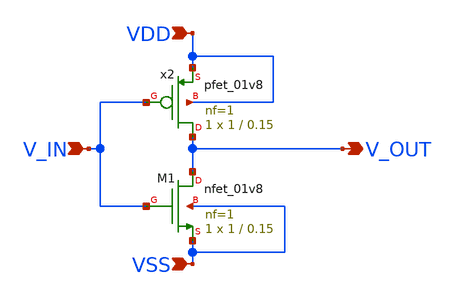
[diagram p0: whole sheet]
** sch_path: schematics_xschem/INV.sch
**.subckt INV V_IN V_OUT VDD VSS
*.ipin V_IN
*.opin V_OUT
*.ipin VDD
*.ipin VSS
XM1 V_OUT V_IN VSS VSS sky130_fd_pr__nfet_01v8 L=0.15 W=1 nf=1 ad='int((nf+1)/2) * W/nf * 0.29' as='int((nf+2)/2) * W/nf * 0.29'
+ pd='2*int((nf+1)/2) * (W/nf + 0.29)' ps='2*int((nf+2)/2) * (W/nf + 0.29)' nrd='0.29 / W' nrs='0.29 / W'
+ sa=0 sb=0 sd=0 mult=1 m=1
Xx2 V_OUT V_IN VDD VDD sky130_fd_pr__pfet_01v8 L=0.15 W=1 nf=1 ad='int((nf+1)/2) * W/nf * 0.29' as='int((nf+2)/2) * W/nf * 0.29'
+ pd='2*int((nf+1)/2) * (W/nf + 0.29)' ps='2*int((nf+2)/2) * (W/nf + 0.29)' nrd='0.29 / W' nrs='0.29 / W'
+ sa=0 sb=0 sd=0 mult=1 m=1
**.ends
.end
